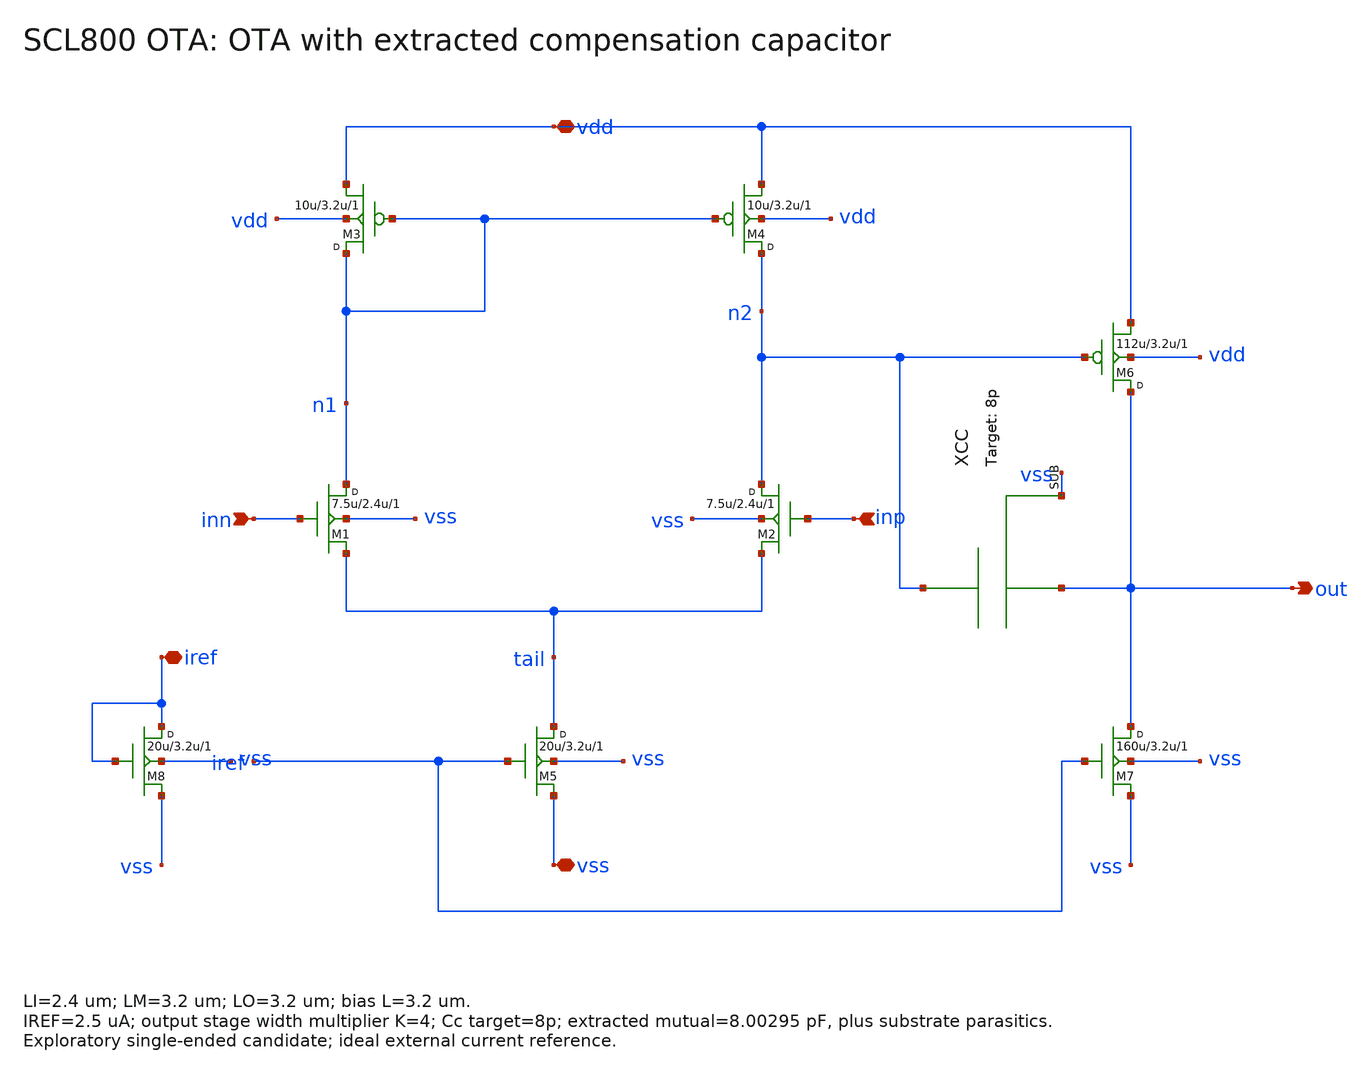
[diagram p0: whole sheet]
** sch_path: OTA/design_2/designs/ota_extracted_cc.sch
**.subckt ota_extracted_cc inp inn out vdd vss iref
*.ipin inp
*.ipin inn
*.opin out
*.iopin vdd
*.iopin vss
*.iopin iref
M3 n1 n1 vdd vdd P w=10u l=3.2u m=1
M4 n2 n1 vdd vdd P w=10u l=3.2u m=1
M1 n1 inn tail vss N w=7.5u l=2.4u m=1
M2 n2 inp tail vss N w=7.5u l=2.4u m=1
M5 tail iref vss vss N w=20u l=3.2u m=1
M6 out n2 vdd vdd P w=112u l=3.2u m=1
M7 out iref vss vss N w=160u l=3.2u m=1
M8 iref iref vss vss N w=20u l=3.2u m=1
XCC n2 out vss scl08_cap_8p
**.ends
.end
